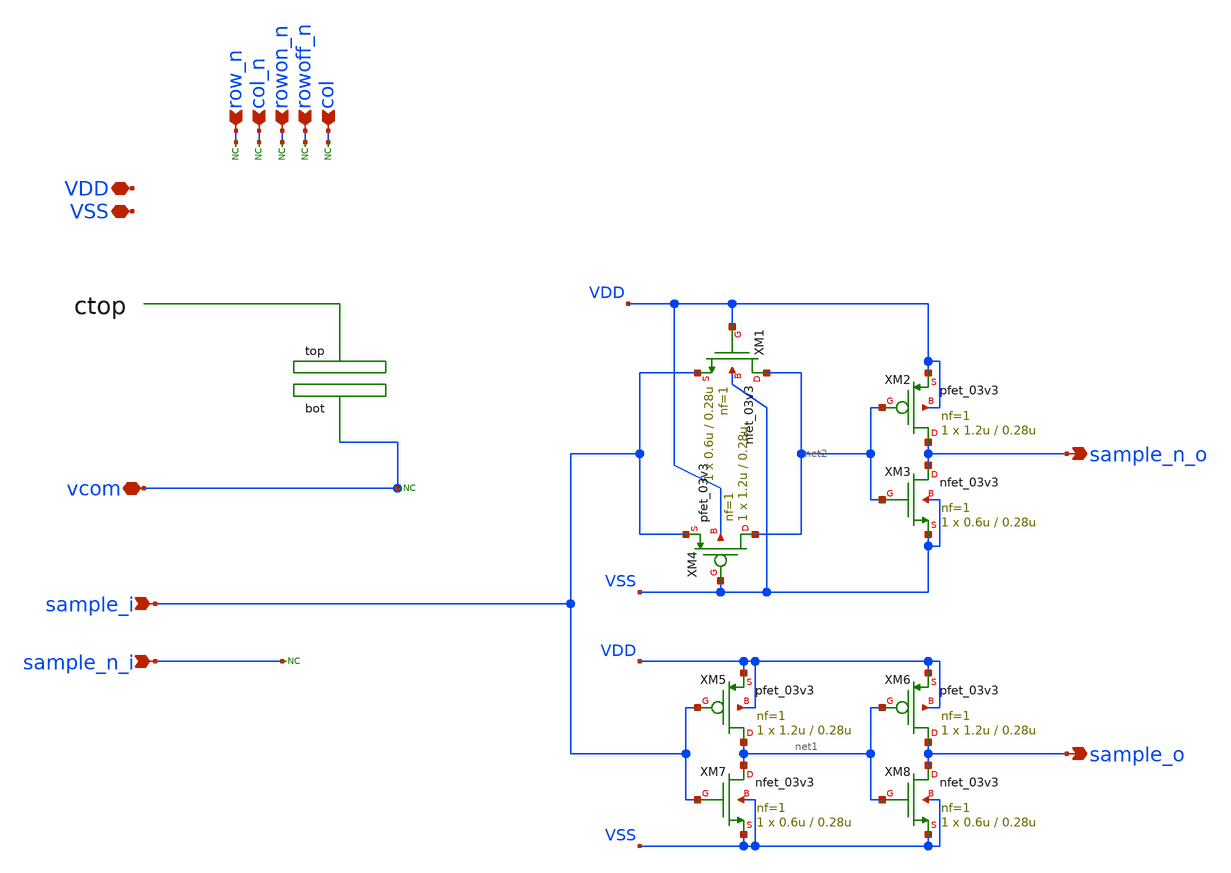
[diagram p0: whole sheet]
** sch_path: adc_sar_array_circuit_drv.sch
**.subckt adc_sar_array_circuit_drv sample_n_i sample_i vcom row_n col_n rowon_n VDD VSS sample_o
*+ sample_n_o rowoff_n col
*.ipin sample_n_i
*.ipin sample_i
*.iopin vcom
*.ipin row_n
*.ipin col_n
*.ipin rowon_n
*.iopin VDD
*.iopin VSS
*.opin sample_o
*.opin sample_n_o
*.ipin rowoff_n
*.ipin col
* noconn row_n
* noconn col_n
* noconn rowon_n
* noconn vcom
* noconn rowoff_n
* noconn col
* noconn sample_n_i
XM1 net2 VDD sample_i VSS nfet_03v3 L=0.28u W=0.6u nf=1 ad='int((nf+1)/2) * W/nf * 0.18u' as='int((nf+2)/2) * W/nf * 0.18u'
+ pd='2*int((nf+1)/2) * (W/nf + 0.18u)' ps='2*int((nf+2)/2) * (W/nf + 0.18u)' nrd='0.18u / W' nrs='0.18u / W'
+ sa=0 sb=0 sd=0 m=1
XM2 sample_n_o net2 VDD VDD pfet_03v3 L=0.28u W=1.2u nf=1 ad='int((nf+1)/2) * W/nf * 0.18u' as='int((nf+2)/2) * W/nf * 0.18u'
+ pd='2*int((nf+1)/2) * (W/nf + 0.18u)' ps='2*int((nf+2)/2) * (W/nf + 0.18u)' nrd='0.18u / W' nrs='0.18u / W'
+ sa=0 sb=0 sd=0 m=1
XM3 sample_n_o net2 VSS VSS nfet_03v3 L=0.28u W=0.6u nf=1 ad='int((nf+1)/2) * W/nf * 0.18u' as='int((nf+2)/2) * W/nf * 0.18u'
+ pd='2*int((nf+1)/2) * (W/nf + 0.18u)' ps='2*int((nf+2)/2) * (W/nf + 0.18u)' nrd='0.18u / W' nrs='0.18u / W'
+ sa=0 sb=0 sd=0 m=1
XM4 net2 VSS sample_i VDD pfet_03v3 L=0.28u W=1.2u nf=1 ad='int((nf+1)/2) * W/nf * 0.18u' as='int((nf+2)/2) * W/nf * 0.18u'
+ pd='2*int((nf+1)/2) * (W/nf + 0.18u)' ps='2*int((nf+2)/2) * (W/nf + 0.18u)' nrd='0.18u / W' nrs='0.18u / W'
+ sa=0 sb=0 sd=0 m=1
XM5 net1 sample_i VDD VDD pfet_03v3 L=0.28u W=1.2u nf=1 ad='int((nf+1)/2) * W/nf * 0.18u' as='int((nf+2)/2) * W/nf * 0.18u'
+ pd='2*int((nf+1)/2) * (W/nf + 0.18u)' ps='2*int((nf+2)/2) * (W/nf + 0.18u)' nrd='0.18u / W' nrs='0.18u / W'
+ sa=0 sb=0 sd=0 m=1
XM6 sample_o net1 VDD VDD pfet_03v3 L=0.28u W=1.2u nf=1 ad='int((nf+1)/2) * W/nf * 0.18u' as='int((nf+2)/2) * W/nf * 0.18u'
+ pd='2*int((nf+1)/2) * (W/nf + 0.18u)' ps='2*int((nf+2)/2) * (W/nf + 0.18u)' nrd='0.18u / W' nrs='0.18u / W'
+ sa=0 sb=0 sd=0 m=1
XM7 net1 sample_i VSS VSS nfet_03v3 L=0.28u W=0.6u nf=1 ad='int((nf+1)/2) * W/nf * 0.18u' as='int((nf+2)/2) * W/nf * 0.18u'
+ pd='2*int((nf+1)/2) * (W/nf + 0.18u)' ps='2*int((nf+2)/2) * (W/nf + 0.18u)' nrd='0.18u / W' nrs='0.18u / W'
+ sa=0 sb=0 sd=0 m=1
XM8 sample_o net1 VSS VSS nfet_03v3 L=0.28u W=0.6u nf=1 ad='int((nf+1)/2) * W/nf * 0.18u' as='int((nf+2)/2) * W/nf * 0.18u'
+ pd='2*int((nf+1)/2) * (W/nf + 0.18u)' ps='2*int((nf+2)/2) * (W/nf + 0.18u)' nrd='0.18u / W' nrs='0.18u / W'
+ sa=0 sb=0 sd=0 m=1
**.ends
.end
